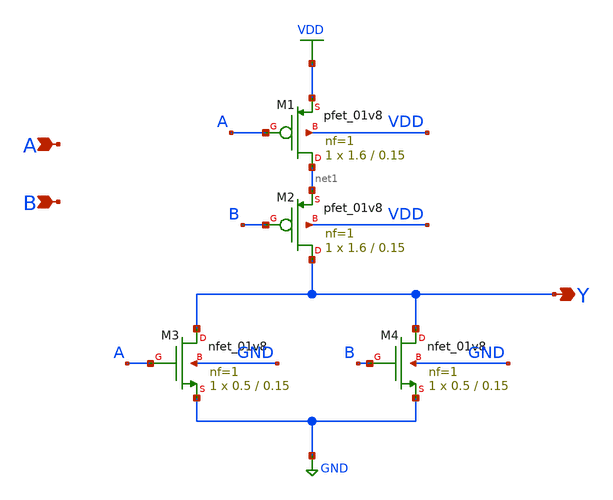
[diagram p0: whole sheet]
** sch_path: eng331lab_final/eng331lab_xschem/nor2.sch
**.subckt nor2 A B Y
*.ipin A
*.ipin B
*.opin Y
XM1 net1 A VDD VDD sky130_fd_pr__pfet_01v8 L=0.15 W=1.6 nf=1 ad='int((1 + 1)/2) * 1.6 / 1 * 0.29' as='int((1 + 2)/2) * 1.6 / 1 * 0.29'
+ pd='2*int((1 + 1)/2) * (1.6 / 1 + 0.29)' ps='2*int((1 + 2)/2) * (1.6 / 1 + 0.29)' nrd='0.29 / 1.6 ' nrs='0.29 / 1.6 '
+ sa=0 sb=0 sd=0 mult=1 m=1
XM2 Y B net1 VDD sky130_fd_pr__pfet_01v8 L=0.15 W=1.6 nf=1 ad='int((1 + 1)/2) * 1.6 / 1 * 0.29' as='int((1 + 2)/2) * 1.6 / 1 * 0.29'
+ pd='2*int((1 + 1)/2) * (1.6 / 1 + 0.29)' ps='2*int((1 + 2)/2) * (1.6 / 1 + 0.29)' nrd='0.29 / 1.6 ' nrs='0.29 / 1.6 '
+ sa=0 sb=0 sd=0 mult=1 m=1
XM3 Y A GND GND sky130_fd_pr__nfet_01v8 L=0.15 W=0.5 nf=1 ad='int((1 + 1)/2) * 0.5 / 1 * 0.29' as='int((1 + 2)/2) * 0.5 / 1 * 0.29'
+ pd='2*int((1 + 1)/2) * (0.5 / 1 + 0.29)' ps='2*int((1 + 2)/2) * (0.5 / 1 + 0.29)' nrd='0.29 / 0.5 ' nrs='0.29 / 0.5 '
+ sa=0 sb=0 sd=0 mult=1 m=1
XM4 Y B GND GND sky130_fd_pr__nfet_01v8 L=0.15 W=0.5 nf=1 ad='int((1 + 1)/2) * 0.5 / 1 * 0.29' as='int((1 + 2)/2) * 0.5 / 1 * 0.29'
+ pd='2*int((1 + 1)/2) * (0.5 / 1 + 0.29)' ps='2*int((1 + 2)/2) * (0.5 / 1 + 0.29)' nrd='0.29 / 0.5 ' nrs='0.29 / 0.5 '
+ sa=0 sb=0 sd=0 mult=1 m=1
**.ends
.GLOBAL VDD
.GLOBAL GND
.end
